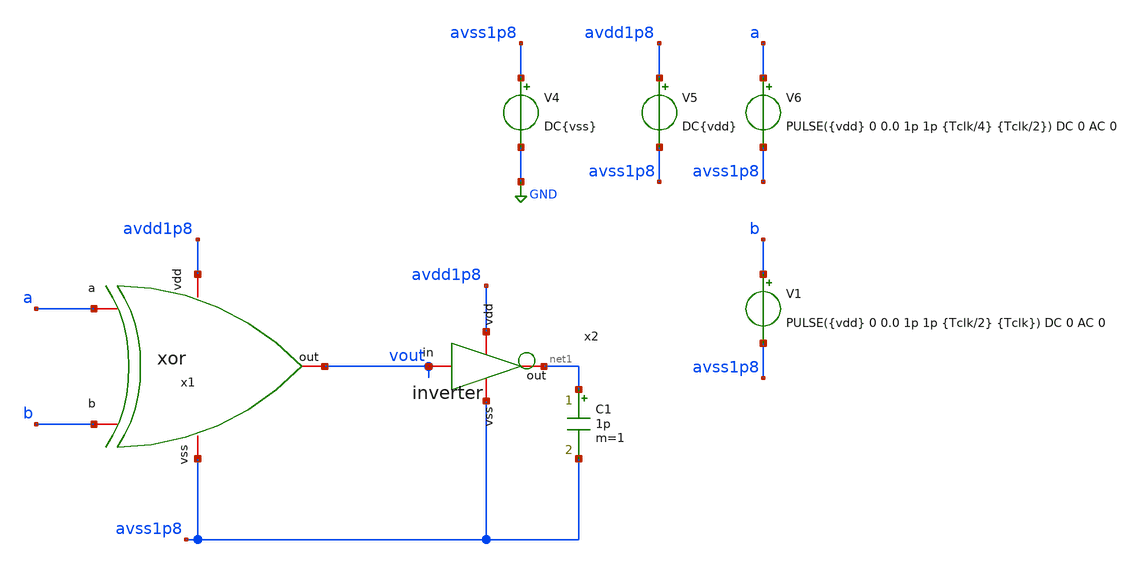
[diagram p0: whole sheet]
** sch_path: verification/testbenches/xor/tb_xor.sch
**.subckt tb_xor
V4 avss1p8 GND DC{vss}
V5 avdd1p8 avss1p8 DC{vdd}
V6 a avss1p8 PULSE({vdd} 0 0.0 1p 1p {Tclk/4} {Tclk/2}) DC 0 AC 0
C1 net1 avss1p8 1p m=1
x2 avdd1p8 net1 vout avss1p8 inverter
V1 b avss1p8 PULSE({vdd} 0 0.0 1p 1p {Tclk/2} {Tclk}) DC 0 AC 0
x1 avdd1p8 a vout b avss1p8 xor
**** begin user architecture code


* Circuit Parameters
.param vdd = 1.2
.param vss = 0.0
.param Tclk = 10n
.options TEMP = 27.0
* Include Models - IHP SG13G2
.lib cornerMOSlv.lib mos_tt
* OP Parameters & Singals to save
.save all
*Simulations
.control
tran 0.01u 20n
setplot tran1
plot v(a) v(b)+1.3 v(vout)+1.3*2
reset
dc V6 0 1.2 0.01
setplot dc
*plot vin vout ylabel vout xlabel vin
set filetype = ascii
write dcsweep.raw
.endc
.end


**** end user architecture code
**.ends

* expanding   symbol:  blocks/inverter/schematic/inverter.sym # of pins=4
** sym_path: design/blocks/inverter/schematic/inverter.sym
** sch_path: design/blocks/inverter/schematic/inverter.sch
.subckt inverter vdd out in vss
*.iopin vdd
*.iopin out
*.iopin vss
*.iopin in
XM1 out in vss vss sg13_lv_nmos w=0.75u l=0.15u ng=1 m=1 mm_ok=1
XM2 out in vdd vdd sg13_lv_pmos w=1.5u l=0.15u ng=1 m=1 mm_ok=1
.ends


* expanding   symbol:  blocks/xorgate/schematic/xor.sym # of pins=5
** sym_path: design/blocks/xorgate/schematic/xor.sym
** sch_path: design/blocks/xorgate/schematic/xor.sch
.subckt xor vdd a out b vss
*.iopin vss
*.iopin vdd
*.iopin a
*.iopin b
*.iopin out
XM1 net1 bb vdd vdd sg13_lv_pmos w=0.75u l=0.15u ng=1 m=1 mm_ok=1
XM2 out ab net2 vss sg13_lv_nmos w=0.75u l=0.15u ng=1 m=1 mm_ok=1
XM3 net1 ab vdd vdd sg13_lv_pmos w=1.5u l=0.15u ng=1 m=1 mm_ok=1
XM4 out a net1 vdd sg13_lv_pmos w=0.75u l=0.15u ng=1 m=1 mm_ok=1
XM5 out b net1 vdd sg13_lv_pmos w=1.5u l=0.15u ng=1 m=1 mm_ok=1
XM6 out a net3 vss sg13_lv_nmos w=1.5u l=0.15u ng=1 m=1 mm_ok=1
x1 vdd ab a vss inverter
x2 vdd bb b vss inverter
XM7 net2 bb vss vss sg13_lv_nmos w=3.0u l=0.15u ng=1 m=1 mm_ok=1
XM8 net3 b vss vss sg13_lv_nmos w=3.0u l=0.15u ng=1 m=1 mm_ok=1
.ends

.GLOBAL GND
.end
